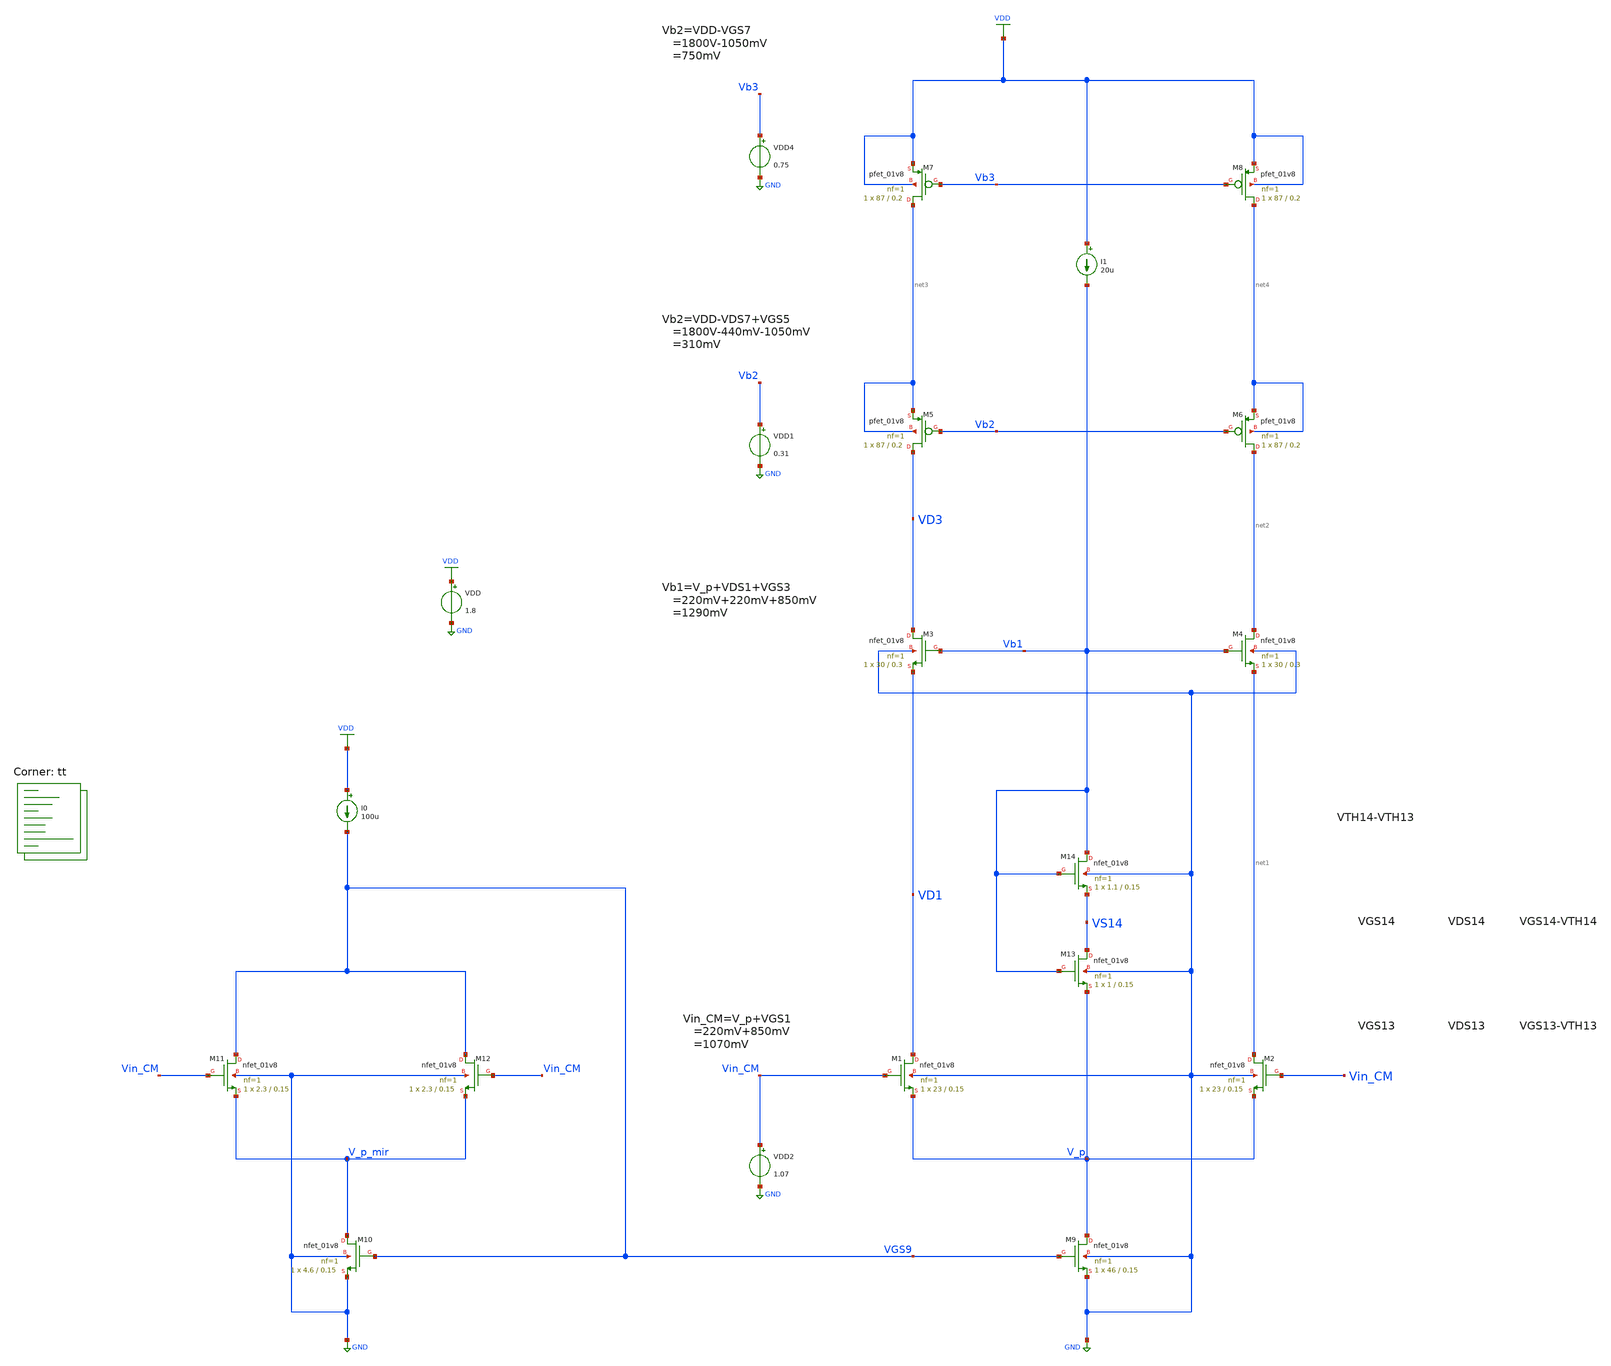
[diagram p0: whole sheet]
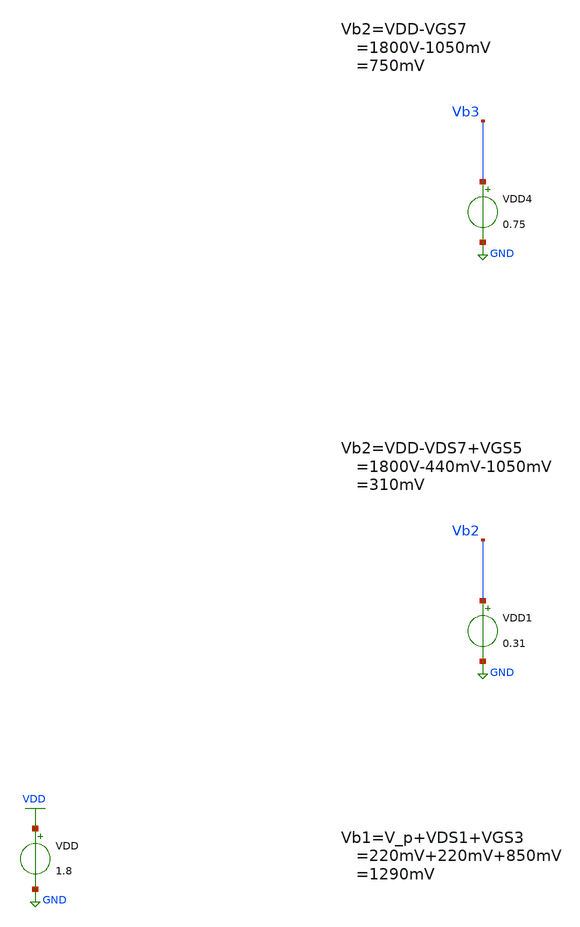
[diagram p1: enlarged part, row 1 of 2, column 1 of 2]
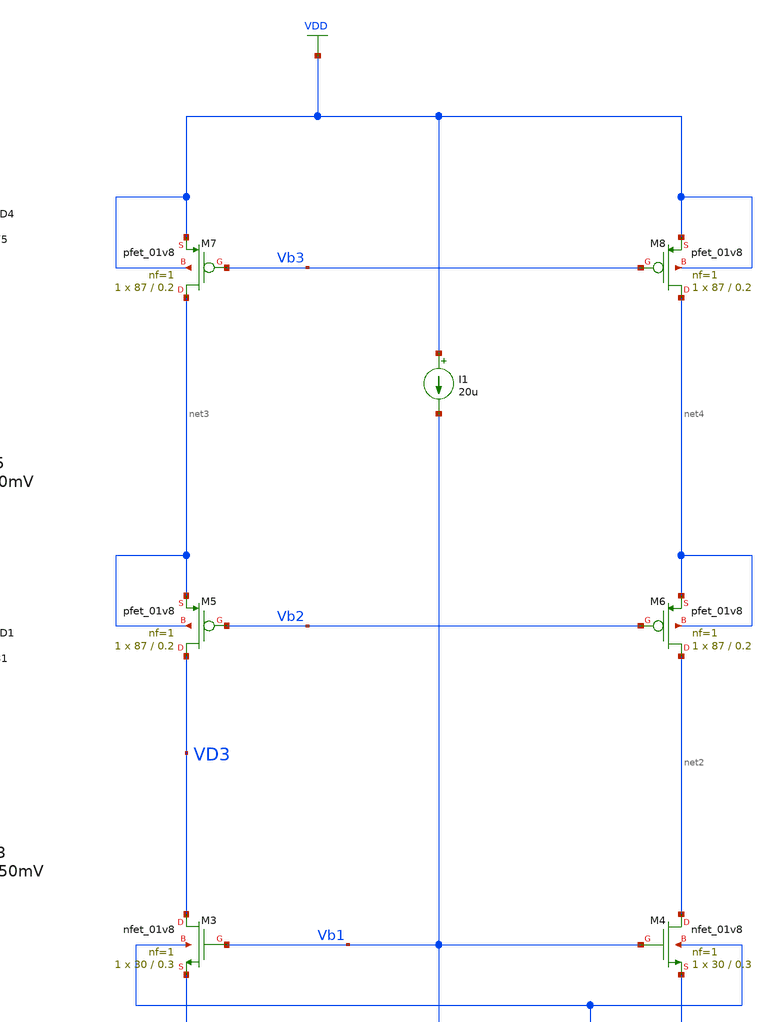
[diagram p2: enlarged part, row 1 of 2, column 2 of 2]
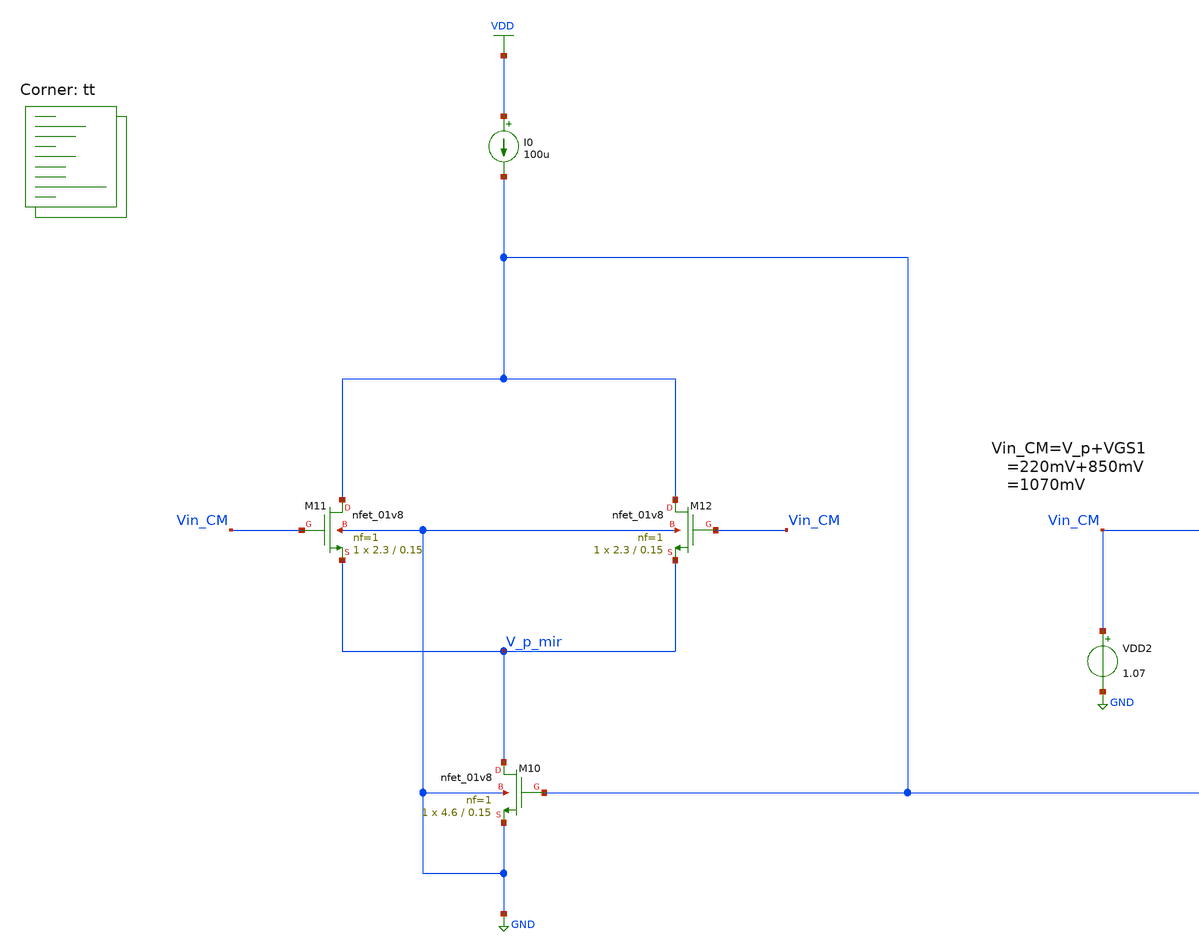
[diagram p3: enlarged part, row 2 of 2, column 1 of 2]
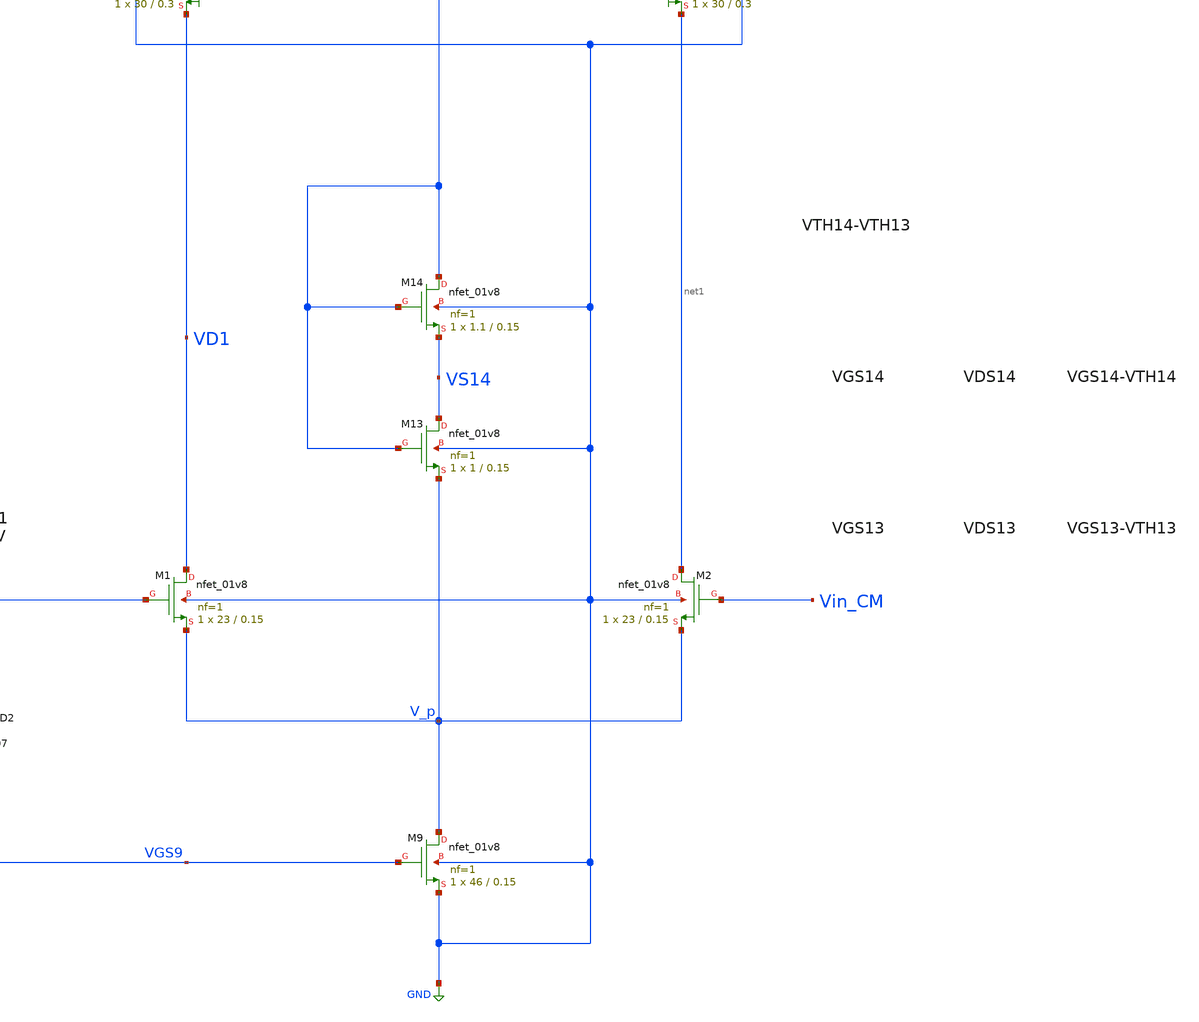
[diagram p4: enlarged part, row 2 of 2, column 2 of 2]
** sch_path: projects/opamp/xschem_ngspice/nfet_vgs_check_vb1.sch
**.subckt nfet_vgs_check_vb1
VDD VDD GND 1.8
XM1 VD1 Vin_CM V_p GND sky130_fd_pr__nfet_01v8 L=0.15 W=23 nf=1 ad='int((nf+1)/2) * W/nf * 0.29' as='int((nf+2)/2) * W/nf * 0.29'
+ pd='2*int((nf+1)/2) * (W/nf + 0.29)' ps='2*int((nf+2)/2) * (W/nf + 0.29)' nrd='0.29 / W' nrs='0.29 / W'
+ sa=0 sb=0 sd=0 mult=1 m=1
XM2 net1 Vin_CM V_p GND sky130_fd_pr__nfet_01v8 L=0.15 W=23 nf=1 ad='int((nf+1)/2) * W/nf * 0.29' as='int((nf+2)/2) * W/nf * 0.29'
+ pd='2*int((nf+1)/2) * (W/nf + 0.29)' ps='2*int((nf+2)/2) * (W/nf + 0.29)' nrd='0.29 / W' nrs='0.29 / W'
+ sa=0 sb=0 sd=0 mult=1 m=1
XM3 VD3 Vb1 VD1 GND sky130_fd_pr__nfet_01v8 L=0.3 W=30 nf=1 ad='int((nf+1)/2) * W/nf * 0.29' as='int((nf+2)/2) * W/nf * 0.29'
+ pd='2*int((nf+1)/2) * (W/nf + 0.29)' ps='2*int((nf+2)/2) * (W/nf + 0.29)' nrd='0.29 / W' nrs='0.29 / W'
+ sa=0 sb=0 sd=0 mult=1 m=1
XM4 net2 Vb1 net1 GND sky130_fd_pr__nfet_01v8 L=0.3 W=30 nf=1 ad='int((nf+1)/2) * W/nf * 0.29' as='int((nf+2)/2) * W/nf * 0.29'
+ pd='2*int((nf+1)/2) * (W/nf + 0.29)' ps='2*int((nf+2)/2) * (W/nf + 0.29)' nrd='0.29 / W' nrs='0.29 / W'
+ sa=0 sb=0 sd=0 mult=1 m=1
XM5 VD3 Vb2 net3 net3 sky130_fd_pr__pfet_01v8 L=0.2 W=87 nf=1 ad='int((nf+1)/2) * W/nf * 0.29' as='int((nf+2)/2) * W/nf * 0.29'
+ pd='2*int((nf+1)/2) * (W/nf + 0.29)' ps='2*int((nf+2)/2) * (W/nf + 0.29)' nrd='0.29 / W' nrs='0.29 / W'
+ sa=0 sb=0 sd=0 mult=1 m=1
XM6 net2 Vb2 net4 net4 sky130_fd_pr__pfet_01v8 L=0.2 W=87 nf=1 ad='int((nf+1)/2) * W/nf * 0.29' as='int((nf+2)/2) * W/nf * 0.29'
+ pd='2*int((nf+1)/2) * (W/nf + 0.29)' ps='2*int((nf+2)/2) * (W/nf + 0.29)' nrd='0.29 / W' nrs='0.29 / W'
+ sa=0 sb=0 sd=0 mult=1 m=1
XM7 net3 Vb3 VDD VDD sky130_fd_pr__pfet_01v8 L=0.2 W=87 nf=1 ad='int((nf+1)/2) * W/nf * 0.29' as='int((nf+2)/2) * W/nf * 0.29'
+ pd='2*int((nf+1)/2) * (W/nf + 0.29)' ps='2*int((nf+2)/2) * (W/nf + 0.29)' nrd='0.29 / W' nrs='0.29 / W'
+ sa=0 sb=0 sd=0 mult=1 m=1
XM8 net4 Vb3 VDD VDD sky130_fd_pr__pfet_01v8 L=0.2 W=87 nf=1 ad='int((nf+1)/2) * W/nf * 0.29' as='int((nf+2)/2) * W/nf * 0.29'
+ pd='2*int((nf+1)/2) * (W/nf + 0.29)' ps='2*int((nf+2)/2) * (W/nf + 0.29)' nrd='0.29 / W' nrs='0.29 / W'
+ sa=0 sb=0 sd=0 mult=1 m=1
XM9 V_p VGS9 GND GND sky130_fd_pr__nfet_01v8 L=0.15 W=46 nf=1 ad='int((nf+1)/2) * W/nf * 0.29' as='int((nf+2)/2) * W/nf * 0.29'
+ pd='2*int((nf+1)/2) * (W/nf + 0.29)' ps='2*int((nf+2)/2) * (W/nf + 0.29)' nrd='0.29 / W' nrs='0.29 / W'
+ sa=0 sb=0 sd=0 mult=1 m=1
VDD2 Vin_CM GND 1.07
VDD1 Vb2 GND 0.31
VDD4 Vb3 GND 0.75
XM10 V_p_mir VGS9 GND GND sky130_fd_pr__nfet_01v8 L=0.15 W=4.6 nf=1 ad='int((nf+1)/2) * W/nf * 0.29'
+ as='int((nf+2)/2) * W/nf * 0.29' pd='2*int((nf+1)/2) * (W/nf + 0.29)' ps='2*int((nf+2)/2) * (W/nf + 0.29)'
+ nrd='0.29 / W' nrs='0.29 / W' sa=0 sb=0 sd=0 mult=1 m=1
I0 VDD VGS9 100u
XM11 VGS9 Vin_CM V_p_mir GND sky130_fd_pr__nfet_01v8 L=0.15 W=2.3 nf=1 ad='int((nf+1)/2) * W/nf * 0.29'
+ as='int((nf+2)/2) * W/nf * 0.29' pd='2*int((nf+1)/2) * (W/nf + 0.29)' ps='2*int((nf+2)/2) * (W/nf + 0.29)'
+ nrd='0.29 / W' nrs='0.29 / W' sa=0 sb=0 sd=0 mult=1 m=1
XM12 VGS9 Vin_CM V_p_mir GND sky130_fd_pr__nfet_01v8 L=0.15 W=2.3 nf=1 ad='int((nf+1)/2) * W/nf * 0.29'
+ as='int((nf+2)/2) * W/nf * 0.29' pd='2*int((nf+1)/2) * (W/nf + 0.29)' ps='2*int((nf+2)/2) * (W/nf + 0.29)'
+ nrd='0.29 / W' nrs='0.29 / W' sa=0 sb=0 sd=0 mult=1 m=1
XM13 VS14 Vb1 V_p GND sky130_fd_pr__nfet_01v8 L=0.15 W=1 nf=1 ad='int((nf+1)/2) * W/nf * 0.29' as='int((nf+2)/2) * W/nf * 0.29'
+ pd='2*int((nf+1)/2) * (W/nf + 0.29)' ps='2*int((nf+2)/2) * (W/nf + 0.29)' nrd='0.29 / W' nrs='0.29 / W'
+ sa=0 sb=0 sd=0 mult=1 m=1
XM14 Vb1 Vb1 VS14 GND sky130_fd_pr__nfet_01v8 L=0.15 W=1.1 nf=1 ad='int((nf+1)/2) * W/nf * 0.29' as='int((nf+2)/2) * W/nf * 0.29'
+ pd='2*int((nf+1)/2) * (W/nf + 0.29)' ps='2*int((nf+2)/2) * (W/nf + 0.29)' nrd='0.29 / W' nrs='0.29 / W'
+ sa=0 sb=0 sd=0 mult=1 m=1
I1 VDD Vb1 20u
**** begin user architecture code



.option method=gear
.option wnflag=1
.option savecurrents

.save @m.xm1.msky130_fd_pr__nfet_01v8[gm] @m.xm2.msky130_fd_pr__nfet_01v8[gm] @m.xm3.msky130_fd_pr__nfet_01v8[gm] @m.xm4.msky130_fd_pr__nfet_01v8[gm] @m.xm5.msky130_fd_pr__nfet_01v8[gm] @m.xm6.msky130_fd_pr__nfet_01v8[gm] @m.xm7.msky130_fd_pr__nfet_01v8[gm] @m.xm8.msky130_fd_pr__nfet_01v8[gm] @m.xm9.msky130_fd_pr__nfet_01v8[gm] @m.xm10.msky130_fd_pr__nfet_01v8[gm] @m.xm11.msky130_fd_pr__nfet_01v8[gm] @m.xm12.msky130_fd_pr__nfet_01v8[gm] @m.xm13.msky130_fd_pr__nfet_01v8[gm] @m.xm14.msky130_fd_pr__nfet_01v8[gm] @m.xm1.msky130_fd_pr__nfet_01v8[vth] @m.xm2.msky130_fd_pr__nfet_01v8[vth] @m.xm3.msky130_fd_pr__nfet_01v8[vth] @m.xm4.msky130_fd_pr__nfet_01v8[vth] @m.xm5.msky130_fd_pr__nfet_01v8[vth] @m.xm6.msky130_fd_pr__nfet_01v8[vth] @m.xm7.msky130_fd_pr__nfet_01v8[vth] @m.xm8.msky130_fd_pr__nfet_01v8[vth] @m.xm9.msky130_fd_pr__nfet_01v8[vth] @m.xm10.msky130_fd_pr__nfet_01v8[vth] @m.xm11.msky130_fd_pr__nfet_01v8[vth] @m.xm12.msky130_fd_pr__nfet_01v8[vth] @m.xm13.msky130_fd_pr__nfet_01v8[vth] @m.xm14.msky130_fd_pr__nfet_01v8[vth]

.control

  save all
  * op
  dc VDD 0 2.0 0.1
  * tran 1ns 12us
  remzerovec
  write nfet_vgs_check_vb1.raw
  set appendwrite

.endc




.lib $::SKYWATER_MODELS/sky130.lib.spice tt
**** end user architecture code
**.ends
.GLOBAL GND
.GLOBAL VDD
.end
